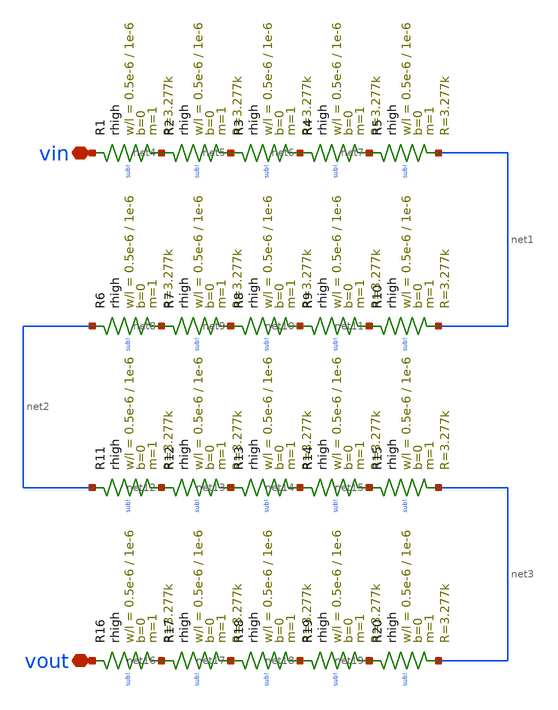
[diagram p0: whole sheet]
** sch_path: LVS/Unic_cass_final_design_lvs/Simulations/Opamp_design/Src/res.sch
**.subckt res vin vout
*.iopin vin
*.iopin vout
XR1 vin net4 sub! rhigh w=0.5e-6 l=1e-6 m=1 b=0 mm_ok=1
XR2 net4 net5 sub! rhigh w=0.5e-6 l=1e-6 m=1 b=0 mm_ok=1
XR3 net5 net6 sub! rhigh w=0.5e-6 l=1e-6 m=1 b=0 mm_ok=1
XR4 net6 net7 sub! rhigh w=0.5e-6 l=1e-6 m=1 b=0 mm_ok=1
XR5 net7 net1 sub! rhigh w=0.5e-6 l=1e-6 m=1 b=0 mm_ok=1
XR6 net2 net8 sub! rhigh w=0.5e-6 l=1e-6 m=1 b=0 mm_ok=1
XR7 net8 net9 sub! rhigh w=0.5e-6 l=1e-6 m=1 b=0 mm_ok=1
XR8 net9 net10 sub! rhigh w=0.5e-6 l=1e-6 m=1 b=0 mm_ok=1
XR9 net10 net11 sub! rhigh w=0.5e-6 l=1e-6 m=1 b=0 mm_ok=1
XR10 net11 net1 sub! rhigh w=0.5e-6 l=1e-6 m=1 b=0 mm_ok=1
XR11 net2 net12 sub! rhigh w=0.5e-6 l=1e-6 m=1 b=0 mm_ok=1
XR12 net12 net13 sub! rhigh w=0.5e-6 l=1e-6 m=1 b=0 mm_ok=1
XR13 net13 net14 sub! rhigh w=0.5e-6 l=1e-6 m=1 b=0 mm_ok=1
XR14 net14 net15 sub! rhigh w=0.5e-6 l=1e-6 m=1 b=0 mm_ok=1
XR15 net15 net3 sub! rhigh w=0.5e-6 l=1e-6 m=1 b=0 mm_ok=1
XR16 vout net16 sub! rhigh w=0.5e-6 l=1e-6 m=1 b=0 mm_ok=1
XR17 net16 net17 sub! rhigh w=0.5e-6 l=1e-6 m=1 b=0 mm_ok=1
XR18 net17 net18 sub! rhigh w=0.5e-6 l=1e-6 m=1 b=0 mm_ok=1
XR19 net18 net19 sub! rhigh w=0.5e-6 l=1e-6 m=1 b=0 mm_ok=1
XR20 net19 net3 sub! rhigh w=0.5e-6 l=1e-6 m=1 b=0 mm_ok=1
**.ends
.end
